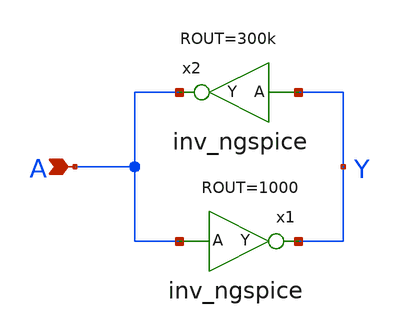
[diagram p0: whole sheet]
** sch_path: xschem_library/ngspice/keeper_ngspice.sch
* Copyright (C) 1998-2023 Stefan Frederik Schippers
* This program is free software; you can redistribute it and/or modify
* it under the terms of the GNU General Public License as published by
* the Free Software Foundation; either version 2 of the License, or
* (at your option) any later version.
* This program is distributed in the hope that it will be useful,
* but WITHOUT ANY WARRANTY; without even the implied warranty of
* MERCHANTABILITY or FITNESS FOR A PARTICULAR PURPOSE.  See the
* GNU General Public License for more details.
* You should have received a copy of the GNU General Public License
* along with this program; if not, write to the Free Software
**.subckt keeper_ngspice A
*.ipin A
x1 Y A inv_ngspice ROUT=1000
x2 A Y inv_ngspice ROUT=300k
**.ends

* expanding   symbol:  inv_ngspice.sym # of pins=2
** sym_path: xschem_library/ngspice/inv_ngspice.sym
** sch_path: xschem_library/ngspice/inv_ngspice.sch
.subckt inv_ngspice Y A  ROUT=1000
*.ipin A
*.opin Y
B1 net1 0 V = 'VCC/2*(1-tanh((V(A1)-VCC/2)*100))'
R1 Y1 net1 'ROUT' m=1
C1 A1 0 8f m=1
C2 Y1 0 8f m=1
V1 Y Y1 0
.save i(v1)
V2 A1 A 0
.save i(v2)
.ends

.end
